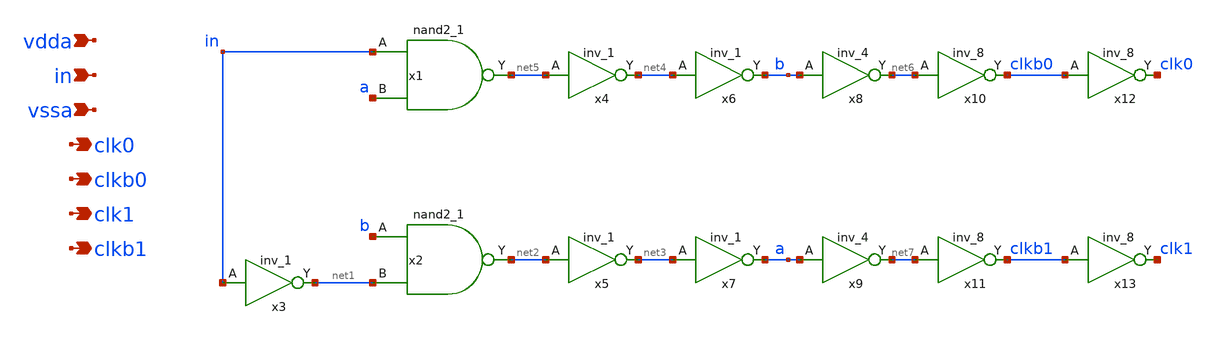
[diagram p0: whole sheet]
** sch_path: xschem/nooverlap_clk.sch
**.subckt nooverlap_clk vdda in vssa clk0 clkb0 clk1 clkb1
*.ipin vdda
*.ipin in
*.ipin vssa
*.opin clk0
*.opin clkb0
*.opin clk1
*.opin clkb1
x1 in a vssa vssa vdda vdda net5 sky130_fd_sc_hdll__nand2_1
x2 b net1 vssa vssa vdda vdda net2 sky130_fd_sc_hdll__nand2_1
x3 in vssa vssa vdda vdda net1 sky130_fd_sc_hdll__inv_1
x4 net5 vssa vssa vdda vdda net4 sky130_fd_sc_hdll__inv_1
x5 net2 vssa vssa vdda vdda net3 sky130_fd_sc_hdll__inv_1
x6 net4 vssa vssa vdda vdda b sky130_fd_sc_hdll__inv_1
x7 net3 vssa vssa vdda vdda a sky130_fd_sc_hdll__inv_1
x8 b vssa vssa vdda vdda net6 sky130_fd_sc_hdll__inv_4
x9 a vssa vssa vdda vdda net7 sky130_fd_sc_hdll__inv_4
x10 net6 vssa vssa vdda vdda clkb0 sky130_fd_sc_hdll__inv_8
x11 net7 vssa vssa vdda vdda clkb1 sky130_fd_sc_hdll__inv_8
x12 clkb0 vssa vssa vdda vdda clk0 sky130_fd_sc_hdll__inv_8
x13 clkb1 vssa vssa vdda vdda clk1 sky130_fd_sc_hdll__inv_8
**.ends
.end
